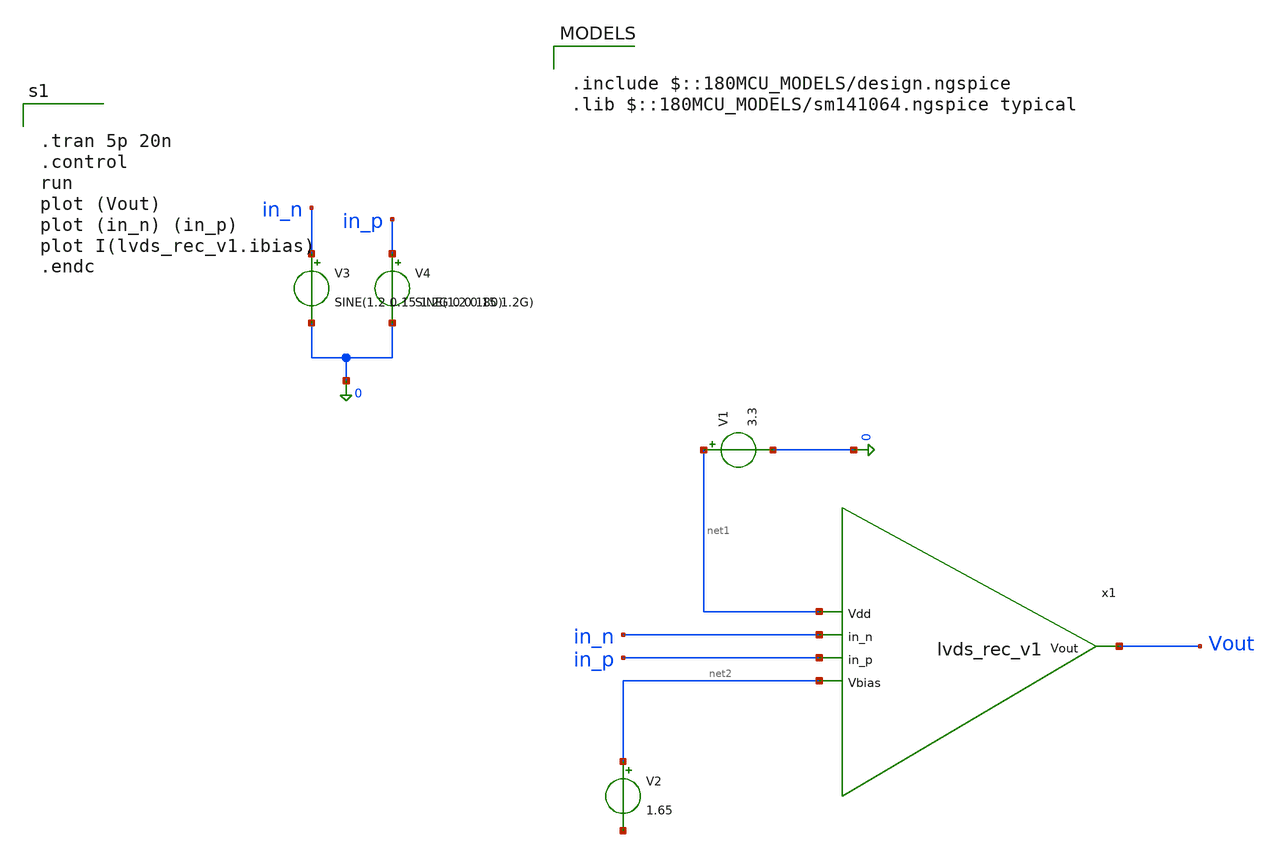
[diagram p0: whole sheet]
** sch_path: blocks/adc/lvds/lvds_rec_test.sch
**.subckt lvds_rec_test
x1 net1 in_n in_p Vout net2 lvds_rec_v1
V1 net1 0 3.3
V2 net2 net3 1.65
V3 in_n 0 SINE(1.2 0.15 1.2G 0 0 180)
V4 in_p 0 SINE(1.2 0.15 1.2G)
**** begin user architecture code

.include $::180MCU_MODELS/design.ngspice
.lib $::180MCU_MODELS/sm141064.ngspice typical



.tran 5p 20n
.control
run
plot (Vout)
plot (in_n) (in_p)
plot I(lvds_rec_v1.ibias)
.endc


**** end user architecture code
**.ends

* expanding   symbol:  lvds_rec_v1.sym # of pins=5
** sym_path: blocks/adc/lvds/lvds_rec_v1.sym
** sch_path: blocks/adc/lvds/lvds_rec_v1.sch
.subckt lvds_rec_v1 Vdd in_n in_p Vout Vbias
*.ipin Vbias
*.ipin Vdd
*.ipin in_n
*.ipin in_p
*.opin Vout
XM1 net1 net1 Vdd Vdd pfet_03v3 L=0.28u W=5u nf=1 ad='int((nf+1)/2) * W/nf * 0.18u' as='int((nf+2)/2) * W/nf * 0.18u'
+ pd='2*int((nf+1)/2) * (W/nf + 0.18u)' ps='2*int((nf+2)/2) * (W/nf + 0.18u)' nrd='0.18u / W' nrs='0.18u / W'
+ sa=0 sb=0 sd=0 m=1
XM2 net4 net1 Vdd Vdd pfet_03v3 L=0.28u W=5u nf=1 ad='int((nf+1)/2) * W/nf * 0.18u' as='int((nf+2)/2) * W/nf * 0.18u'
+ pd='2*int((nf+1)/2) * (W/nf + 0.18u)' ps='2*int((nf+2)/2) * (W/nf + 0.18u)' nrd='0.18u / W' nrs='0.18u / W'
+ sa=0 sb=0 sd=0 m=1
XM3 net1 Vbias 0 0 nfet_03v3 L=0.28u W=1u nf=1 ad='int((nf+1)/2) * W/nf * 0.18u' as='int((nf+2)/2) * W/nf * 0.18u'
+ pd='2*int((nf+1)/2) * (W/nf + 0.18u)' ps='2*int((nf+2)/2) * (W/nf + 0.18u)' nrd='0.18u / W' nrs='0.18u / W'
+ sa=0 sb=0 sd=0 m=3
XM4 Vbias Vbias 0 0 nfet_03v3 L=0.28u W=1u nf=1 ad='int((nf+1)/2) * W/nf * 0.18u' as='int((nf+2)/2) * W/nf * 0.18u'
+ pd='2*int((nf+1)/2) * (W/nf + 0.18u)' ps='2*int((nf+2)/2) * (W/nf + 0.18u)' nrd='0.18u / W' nrs='0.18u / W'
+ sa=0 sb=0 sd=0 m=3
XM5 net2 net2 Vdd Vdd pfet_03v3 L=0.28u W=0.22u nf=1 ad='int((nf+1)/2) * W/nf * 0.18u' as='int((nf+2)/2) * W/nf * 0.18u'
+ pd='2*int((nf+1)/2) * (W/nf + 0.18u)' ps='2*int((nf+2)/2) * (W/nf + 0.18u)' nrd='0.18u / W' nrs='0.18u / W'
+ sa=0 sb=0 sd=0 m=1
XM6 net2 net3 0 0 nfet_03v3 L=0.28u W=0.22u nf=1 ad='int((nf+1)/2) * W/nf * 0.18u' as='int((nf+2)/2) * W/nf * 0.18u'
+ pd='2*int((nf+1)/2) * (W/nf + 0.18u)' ps='2*int((nf+2)/2) * (W/nf + 0.18u)' nrd='0.18u / W' nrs='0.18u / W'
+ sa=0 sb=0 sd=0 m=1
XM7 net3 in_p net4 Vdd pfet_03v3 L=0.28u W=5u nf=1 ad='int((nf+1)/2) * W/nf * 0.18u' as='int((nf+2)/2) * W/nf * 0.18u'
+ pd='2*int((nf+1)/2) * (W/nf + 0.18u)' ps='2*int((nf+2)/2) * (W/nf + 0.18u)' nrd='0.18u / W' nrs='0.18u / W'
+ sa=0 sb=0 sd=0 m=1
XM8 net5 net9 net4 Vdd pfet_03v3 L=0.28u W=0.22u nf=1 ad='int((nf+1)/2) * W/nf * 0.18u' as='int((nf+2)/2) * W/nf * 0.18u'
+ pd='2*int((nf+1)/2) * (W/nf + 0.18u)' ps='2*int((nf+2)/2) * (W/nf + 0.18u)' nrd='0.18u / W' nrs='0.18u / W'
+ sa=0 sb=0 sd=0 m=1
XM9 net6 net10 net4 Vdd pfet_03v3 L=0.28u W=0.22u nf=1 ad='int((nf+1)/2) * W/nf * 0.18u' as='int((nf+2)/2) * W/nf * 0.18u'
+ pd='2*int((nf+1)/2) * (W/nf + 0.18u)' ps='2*int((nf+2)/2) * (W/nf + 0.18u)' nrd='0.18u / W' nrs='0.18u / W'
+ sa=0 sb=0 sd=0 m=1
XM10 net7 in_n net4 Vdd pfet_03v3 L=0.28u W=5u nf=1 ad='int((nf+1)/2) * W/nf * 0.18u' as='int((nf+2)/2) * W/nf * 0.18u'
+ pd='2*int((nf+1)/2) * (W/nf + 0.18u)' ps='2*int((nf+2)/2) * (W/nf + 0.18u)' nrd='0.18u / W' nrs='0.18u / W'
+ sa=0 sb=0 sd=0 m=1
XM11 net3 net3 0 net11 nfet_03v3 L=0.28u W=0.22u nf=1 ad='int((nf+1)/2) * W/nf * 0.18u' as='int((nf+2)/2) * W/nf * 0.18u'
+ pd='2*int((nf+1)/2) * (W/nf + 0.18u)' ps='2*int((nf+2)/2) * (W/nf + 0.18u)' nrd='0.18u / W' nrs='0.18u / W'
+ sa=0 sb=0 sd=0 m=1
XM12 net3 in_p net5 Vdd pfet_03v3 L=0.28u W=1u nf=1 ad='int((nf+1)/2) * W/nf * 0.18u' as='int((nf+2)/2) * W/nf * 0.18u'
+ pd='2*int((nf+1)/2) * (W/nf + 0.18u)' ps='2*int((nf+2)/2) * (W/nf + 0.18u)' nrd='0.18u / W' nrs='0.18u / W'
+ sa=0 sb=0 sd=0 m=1
XM13 net7 in_n net6 Vdd pfet_03v3 L=0.28u W=1u nf=1 ad='int((nf+1)/2) * W/nf * 0.18u' as='int((nf+2)/2) * W/nf * 0.18u'
+ pd='2*int((nf+1)/2) * (W/nf + 0.18u)' ps='2*int((nf+2)/2) * (W/nf + 0.18u)' nrd='0.18u / W' nrs='0.18u / W'
+ sa=0 sb=0 sd=0 m=1
XM14 net7 net7 0 0 nfet_03v3 L=0.28u W=0.22u nf=1 ad='int((nf+1)/2) * W/nf * 0.18u' as='int((nf+2)/2) * W/nf * 0.18u'
+ pd='2*int((nf+1)/2) * (W/nf + 0.18u)' ps='2*int((nf+2)/2) * (W/nf + 0.18u)' nrd='0.18u / W' nrs='0.18u / W'
+ sa=0 sb=0 sd=0 m=1
XM15 net8 net7 0 0 nfet_03v3 L=0.28u W=0.22u nf=1 ad='int((nf+1)/2) * W/nf * 0.18u' as='int((nf+2)/2) * W/nf * 0.18u'
+ pd='2*int((nf+1)/2) * (W/nf + 0.18u)' ps='2*int((nf+2)/2) * (W/nf + 0.18u)' nrd='0.18u / W' nrs='0.18u / W'
+ sa=0 sb=0 sd=0 m=1
XM16 net8 net2 Vdd Vdd pfet_03v3 L=0.28u W=0.22u nf=1 ad='int((nf+1)/2) * W/nf * 0.18u' as='int((nf+2)/2) * W/nf * 0.18u'
+ pd='2*int((nf+1)/2) * (W/nf + 0.18u)' ps='2*int((nf+2)/2) * (W/nf + 0.18u)' nrd='0.18u / W' nrs='0.18u / W'
+ sa=0 sb=0 sd=0 m=1
XM17 net9 net8 0 0 nfet_03v3 L=0.28u W=0.22u nf=1 ad='int((nf+1)/2) * W/nf * 0.18u' as='int((nf+2)/2) * W/nf * 0.18u'
+ pd='2*int((nf+1)/2) * (W/nf + 0.18u)' ps='2*int((nf+2)/2) * (W/nf + 0.18u)' nrd='0.18u / W' nrs='0.18u / W'
+ sa=0 sb=0 sd=0 m=1
XM18 net9 net8 Vdd Vdd pfet_03v3 L=0.28u W=0.22u nf=1 ad='int((nf+1)/2) * W/nf * 0.18u' as='int((nf+2)/2) * W/nf * 0.18u'
+ pd='2*int((nf+1)/2) * (W/nf + 0.18u)' ps='2*int((nf+2)/2) * (W/nf + 0.18u)' nrd='0.18u / W' nrs='0.18u / W'
+ sa=0 sb=0 sd=0 m=1
XM19 net10 net9 0 0 nfet_03v3 L=0.28u W=0.22u nf=1 ad='int((nf+1)/2) * W/nf * 0.18u' as='int((nf+2)/2) * W/nf * 0.18u'
+ pd='2*int((nf+1)/2) * (W/nf + 0.18u)' ps='2*int((nf+2)/2) * (W/nf + 0.18u)' nrd='0.18u / W' nrs='0.18u / W'
+ sa=0 sb=0 sd=0 m=1
XM20 net10 net9 Vdd Vdd pfet_03v3 L=0.28u W=0.22u nf=1 ad='int((nf+1)/2) * W/nf * 0.18u' as='int((nf+2)/2) * W/nf * 0.18u'
+ pd='2*int((nf+1)/2) * (W/nf + 0.18u)' ps='2*int((nf+2)/2) * (W/nf + 0.18u)' nrd='0.18u / W' nrs='0.18u / W'
+ sa=0 sb=0 sd=0 m=1
XM21 Vout net10 0 0 nfet_03v3 L=0.28u W=0.22u nf=1 ad='int((nf+1)/2) * W/nf * 0.18u' as='int((nf+2)/2) * W/nf * 0.18u'
+ pd='2*int((nf+1)/2) * (W/nf + 0.18u)' ps='2*int((nf+2)/2) * (W/nf + 0.18u)' nrd='0.18u / W' nrs='0.18u / W'
+ sa=0 sb=0 sd=0 m=1
XM22 Vout net10 Vdd Vdd pfet_03v3 L=0.28u W=0.22u nf=1 ad='int((nf+1)/2) * W/nf * 0.18u' as='int((nf+2)/2) * W/nf * 0.18u'
+ pd='2*int((nf+1)/2) * (W/nf + 0.18u)' ps='2*int((nf+2)/2) * (W/nf + 0.18u)' nrd='0.18u / W' nrs='0.18u / W'
+ sa=0 sb=0 sd=0 m=1
.ends

.end
